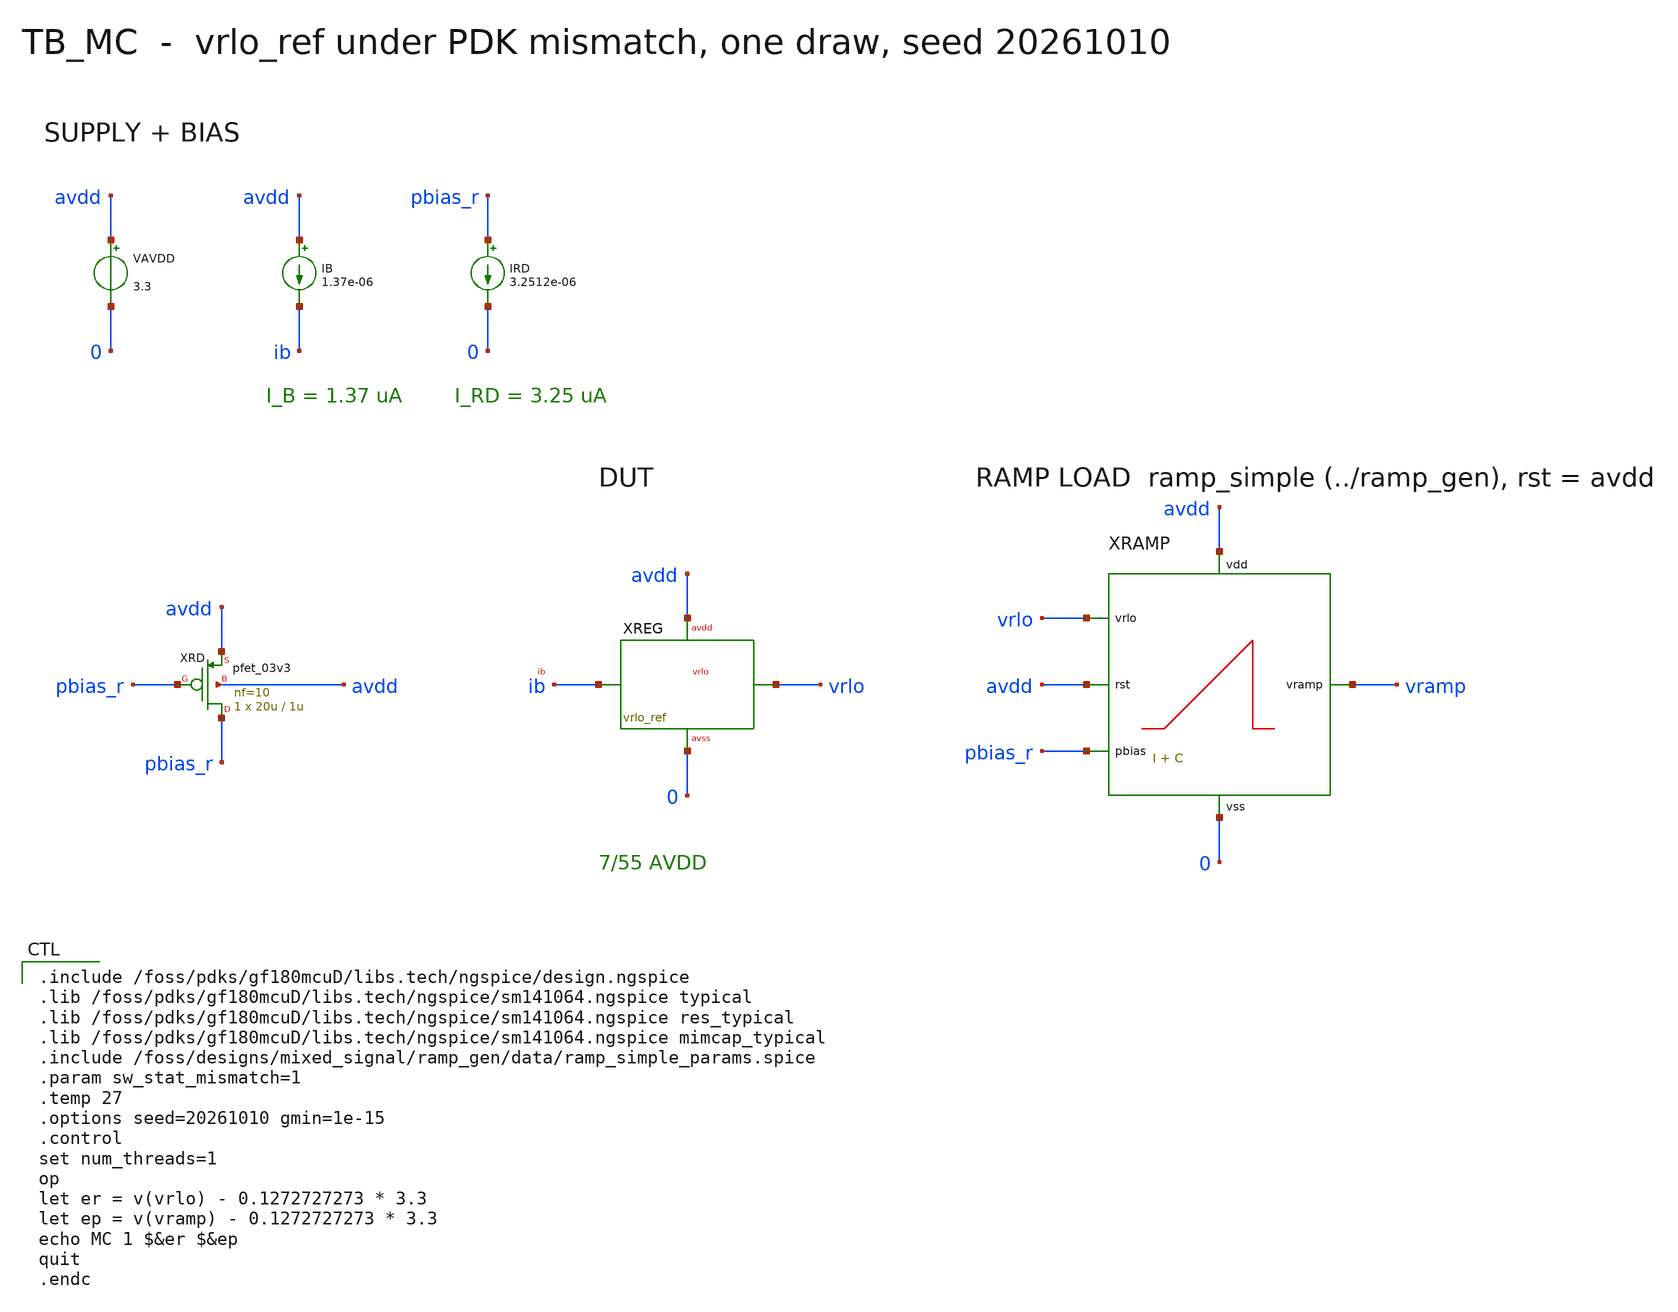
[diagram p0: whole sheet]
** sch_path: mixed_signal/vrlo_ref/tb_mc.sch
**.subckt tb_mc
VAVDD avdd 0 3.3
IB avdd ib 1.37e-06
XREG vrlo ib avdd 0 vrlo_ref
IRD pbias_r 0 3.2512e-06
XRD pbias_r pbias_r avdd avdd pfet_03v3 L=1u W=20u nf=10 m=1
XRAMP vramp avdd vrlo pbias_r avdd 0 ramp_simple
**** begin user architecture code

.include /foss/pdks/gf180mcuD/libs.tech/ngspice/design.ngspice
.lib /foss/pdks/gf180mcuD/libs.tech/ngspice/sm141064.ngspice typical
.lib /foss/pdks/gf180mcuD/libs.tech/ngspice/sm141064.ngspice res_typical
.lib /foss/pdks/gf180mcuD/libs.tech/ngspice/sm141064.ngspice mimcap_typical
.include /foss/designs/mixed_signal/ramp_gen/data/ramp_simple_params.spice
.param sw_stat_mismatch=1
.temp 27
.options seed=20261010 gmin=1e-15
.control
set num_threads=1
op
let er = v(vrlo) - 0.1272727273 * 3.3
let ep = v(vramp) - 0.1272727273 * 3.3
echo MC 1 $&er $&ep
quit
.endc

**** end user architecture code
**.ends
.end
